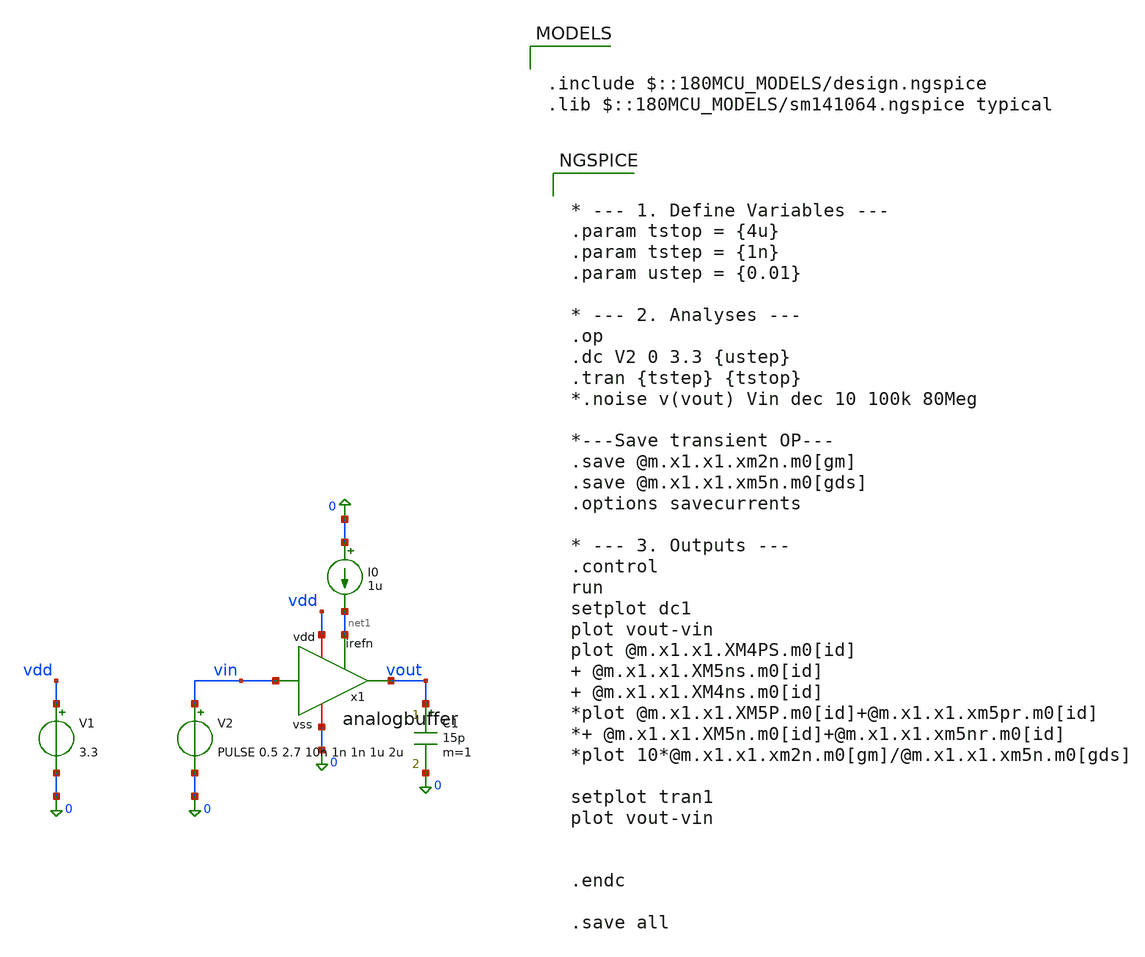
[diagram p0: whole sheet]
** sch_path: General/ADC/analogbuffer/analogbuffer-tb.sch
**.subckt analogbuffer-tb
x1 vdd net1 vin vout 0 analogbuffer
I0 0 net1 1u
V1 vdd 0 3.3
V2 vin 0 PULSE 0.5 2.7 10n 1n 1n 1u 2u
C1 vout 0 15p m=1
**** begin user architecture code


* --- 1. Define Variables ---
.param tstop = {4u}
.param tstep = {1n}
.param ustep = {0.01}

* --- 2. Analyses ---
.op
.dc V2 0 3.3 {ustep}
.tran {tstep} {tstop}
*.noise v(vout) Vin dec 10 100k 80Meg

*---Save transient OP---
.save @m.x1.x1.xm2n.m0[gm]
.save @m.x1.x1.xm5n.m0[gds]
.options savecurrents

* --- 3. Outputs ---
.control
run
setplot dc1
plot vout-vin
plot @m.x1.x1.XM4PS.m0[id]  @m.x1.x1.XM5ns.m0[id]  @m.x1.x1.XM4ns.m0[id]
*plot @m.x1.x1.XM5P.m0[id]+@m.x1.x1.xm5pr.m0[id]
*+ @m.x1.x1.XM5n.m0[id]+@m.x1.x1.xm5nr.m0[id]
*plot 10*@m.x1.x1.xm2n.m0[gm]/@m.x1.x1.xm5n.m0[gds]

setplot tran1
plot vout-vin


.endc

.save all



.include $::180MCU_MODELS/design.ngspice
.lib $::180MCU_MODELS/sm141064.ngspice typical

**** end user architecture code
**.ends
.end
